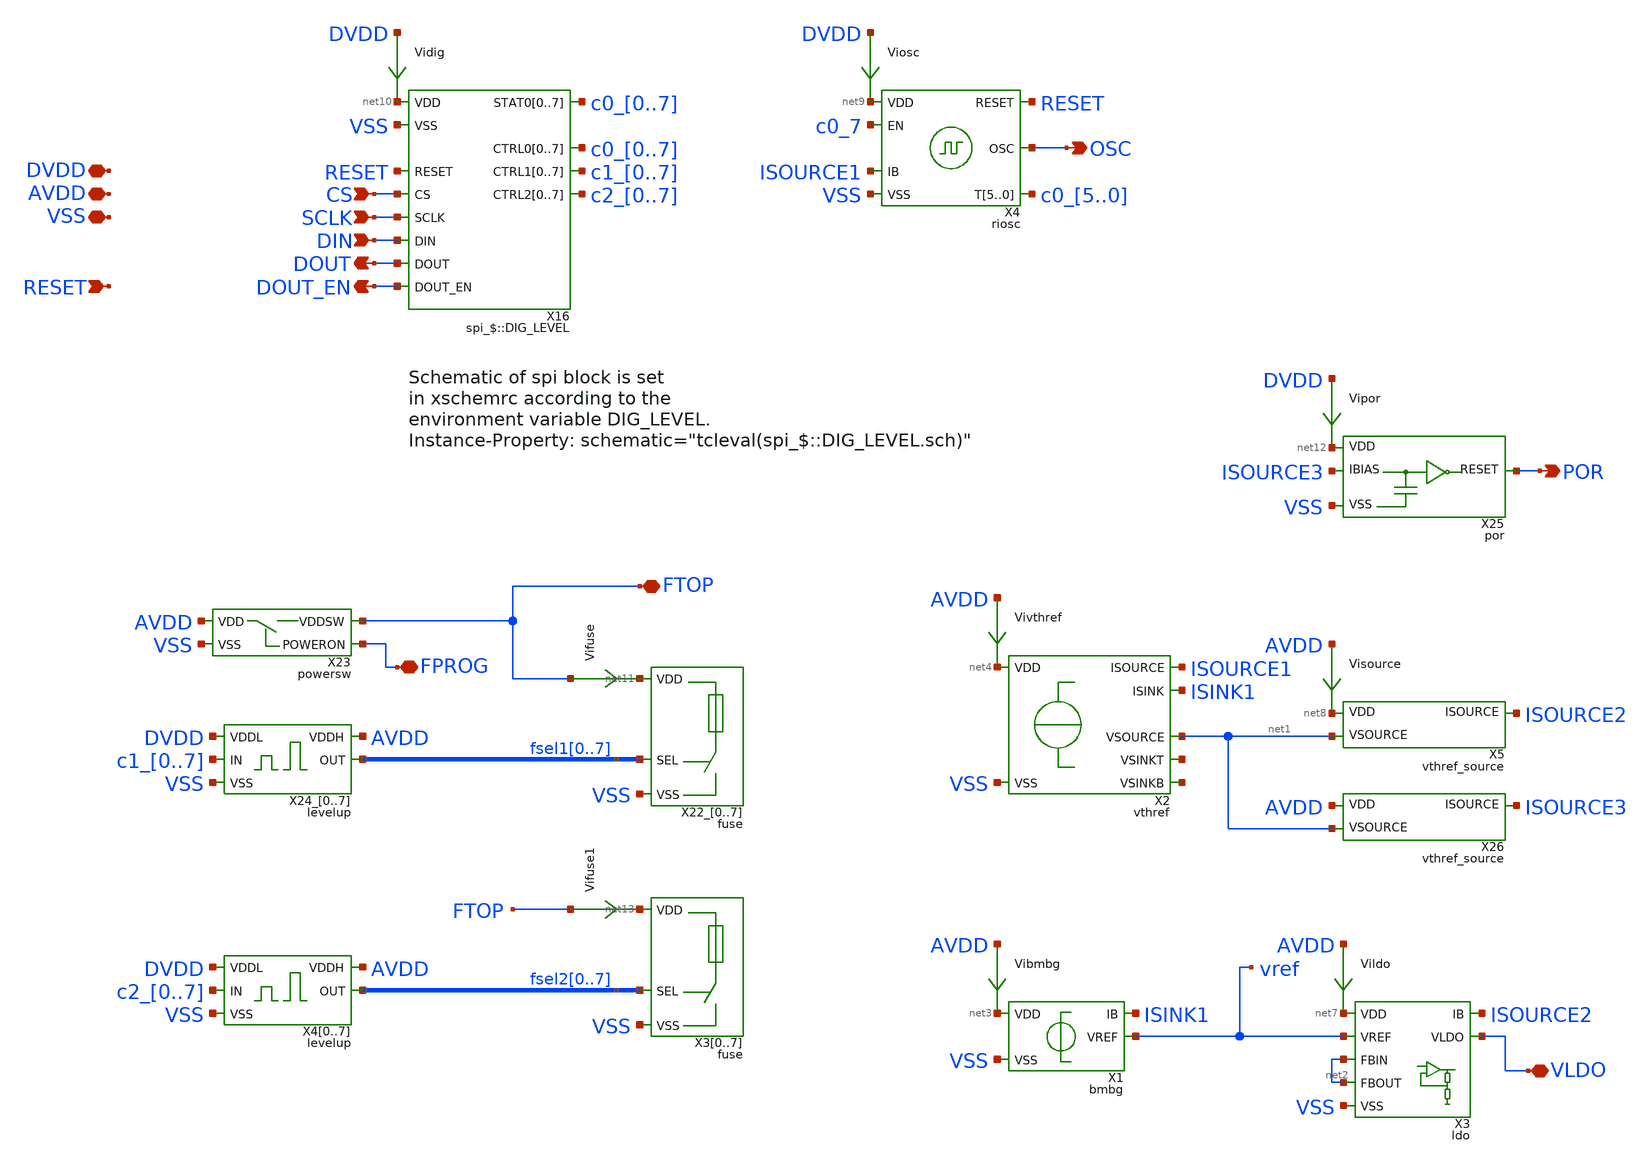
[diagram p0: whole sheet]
** sch_path: xschem/core.sch
**.subckt core VLDO DIN OSC DOUT SCLK CS FTOP FPROG DVDD VSS AVDD POR DOUT_EN RESET
*.iopin VLDO
*.ipin DIN
*.opin OSC
*.opin DOUT
*.ipin SCLK
*.ipin CS
*.iopin FTOP
*.iopin FPROG
*.iopin DVDD
*.iopin VSS
*.iopin AVDD
*.opin POR
*.opin DOUT_EN
*.ipin RESET
X1 net3 VSS ISINK1 vref bmbg
X2 net4 VSS ISOURCE1 ISINK1 net1 net6 net5 vthref
X3 net7 VSS ISOURCE2 vref VLDO net2 net2 ldo
X5 net8 ISOURCE2 net1 vthref_source
Vivthref AVDD net4 0
.save i(vivthref)
Viosc DVDD net9 0
.save i(viosc)
Vibmbg AVDD net3 0
.save i(vibmbg)
Vildo AVDD net7 0
.save i(vildo)
Vidig DVDD net10 0
.save i(vidig)
X16 DOUT_EN RESET CS c0_0 c0_1 c0_2 c0_3 c0_4 c0_5 c0_6 c0_7 c1_0 c1_1 c1_2 c1_3 c1_4 c1_5 c1_6 c1_7
+ c2_0 c2_1 c2_2 c2_3 c2_4 c2_5 c2_6 c2_7 SCLK DIN DOUT c0_0 c0_1 c0_2 c0_3 c0_4 c0_5 c0_6 c0_7 net10 VSS
+ spi_$::DIG_LEVEL
X4 net9 VSS OSC c0_7 ISOURCE1 RESET c0_5 c0_4 c0_3 c0_2 c0_1 c0_0 riosc
X22_0 net11 VSS fsel10 fuse
X22_1 net11 VSS fsel11 fuse
X22_2 net11 VSS fsel12 fuse
X22_3 net11 VSS fsel13 fuse
X22_4 net11 VSS fsel14 fuse
X22_5 net11 VSS fsel15 fuse
X22_6 net11 VSS fsel16 fuse
X22_7 net11 VSS fsel17 fuse
X23 AVDD FPROG FTOP VSS powersw
X24_0 DVDD VSS c1_0 AVDD fsel10 levelup
X24_1 DVDD VSS c1_1 AVDD fsel11 levelup
X24_2 DVDD VSS c1_2 AVDD fsel12 levelup
X24_3 DVDD VSS c1_3 AVDD fsel13 levelup
X24_4 DVDD VSS c1_4 AVDD fsel14 levelup
X24_5 DVDD VSS c1_5 AVDD fsel15 levelup
X24_6 DVDD VSS c1_6 AVDD fsel16 levelup
X24_7 DVDD VSS c1_7 AVDD fsel17 levelup
Vifuse FTOP net11 0
.save i(vifuse)
Visource AVDD net8 0
.save i(visource)
X25 net12 VSS POR ISOURCE3 por
Vipor DVDD net12 0
.save i(vipor)
X26 AVDD ISOURCE3 net1 vthref_source
X30 net13 VSS fsel20 fuse
X31 net13 VSS fsel21 fuse
X32 net13 VSS fsel22 fuse
X33 net13 VSS fsel23 fuse
X34 net13 VSS fsel24 fuse
X35 net13 VSS fsel25 fuse
X36 net13 VSS fsel26 fuse
X37 net13 VSS fsel27 fuse
X40 DVDD VSS c2_0 AVDD fsel20 levelup
X41 DVDD VSS c2_1 AVDD fsel21 levelup
X42 DVDD VSS c2_2 AVDD fsel22 levelup
X43 DVDD VSS c2_3 AVDD fsel23 levelup
X44 DVDD VSS c2_4 AVDD fsel24 levelup
X45 DVDD VSS c2_5 AVDD fsel25 levelup
X46 DVDD VSS c2_6 AVDD fsel26 levelup
X47 DVDD VSS c2_7 AVDD fsel27 levelup
Vifuse1 FTOP net13 0
.save i(vifuse1)
**** begin user architecture code

.include ${::IHP_STDCELLS}/sg13g2_stdcell.spice

.subckt sg13g2_not_1 Y A VDD VSS
XX1 Y A VSS VSS sg13_lv_nmos w=740.00n l=130.00n ng=1 ad=2.516e-13 as=2.516e-13 pd=2.16e-06
+ ps=2.16e-06 m=1
XX0 Y A VDD VDD sg13_lv_pmos w=1.12u l=130.00n ng=1 ad=3.808e-13 as=3.808e-13 pd=2.92e-06
+ ps=2.92e-06 m=1
.ends

**** end user architecture code
**.ends
.end
